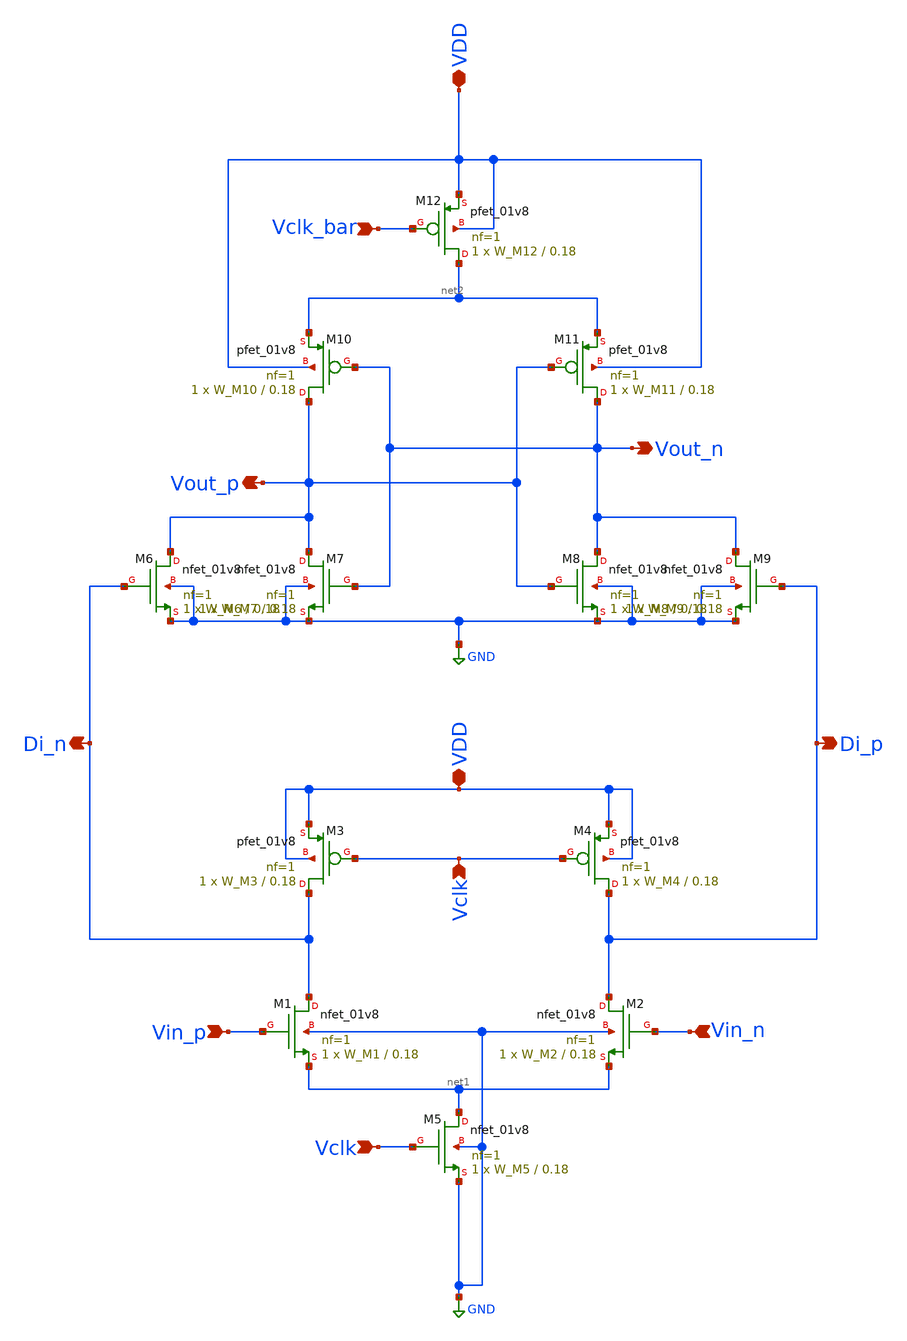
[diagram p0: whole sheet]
** sch_path: xschem/double_tail_comp.sch
**.subckt double_tail_comp VDD Vclk Vclk Vin_p Vin_n Di_n Di_p Vout_n Vout_p Vclk_bar VDD
*.iopin VDD
*.ipin Vclk
*.ipin Vclk
*.ipin Vin_p
*.ipin Vin_n
*.opin Di_n
*.opin Di_p
*.opin Vout_n
*.opin Vout_p
*.ipin Vclk_bar
*.iopin VDD
XM1 Di_n Vin_p net1 GND sky130_fd_pr__nfet_01v8 L=0.18 W=W_M1 nf=1 ad='int((nf+1)/2) * W/nf * 0.29' as='int((nf+2)/2) * W/nf * 0.29'
+ pd='2*int((nf+1)/2) * (W/nf + 0.29)' ps='2*int((nf+2)/2) * (W/nf + 0.29)' nrd='0.29 / W' nrs='0.29 / W'
+ sa=0 sb=0 sd=0 mult=1 m=1
XM2 Di_p Vin_n net1 GND sky130_fd_pr__nfet_01v8 L=0.18 W=W_M2 nf=1 ad='int((nf+1)/2) * W/nf * 0.29' as='int((nf+2)/2) * W/nf * 0.29'
+ pd='2*int((nf+1)/2) * (W/nf + 0.29)' ps='2*int((nf+2)/2) * (W/nf + 0.29)' nrd='0.29 / W' nrs='0.29 / W'
+ sa=0 sb=0 sd=0 mult=1 m=1
XM3 Di_n Vclk VDD VDD sky130_fd_pr__pfet_01v8 L=0.18 W=W_M3 nf=1 ad='int((nf+1)/2) * W/nf * 0.29' as='int((nf+2)/2) * W/nf * 0.29'
+ pd='2*int((nf+1)/2) * (W/nf + 0.29)' ps='2*int((nf+2)/2) * (W/nf + 0.29)' nrd='0.29 / W' nrs='0.29 / W'
+ sa=0 sb=0 sd=0 mult=1 m=1
XM4 Di_p Vclk VDD VDD sky130_fd_pr__pfet_01v8 L=0.18 W=W_M4 nf=1 ad='int((nf+1)/2) * W/nf * 0.29' as='int((nf+2)/2) * W/nf * 0.29'
+ pd='2*int((nf+1)/2) * (W/nf + 0.29)' ps='2*int((nf+2)/2) * (W/nf + 0.29)' nrd='0.29 / W' nrs='0.29 / W'
+ sa=0 sb=0 sd=0 mult=1 m=1
XM5 net1 Vclk GND GND sky130_fd_pr__nfet_01v8 L=0.18 W=W_M5 nf=1 ad='int((nf+1)/2) * W/nf * 0.29' as='int((nf+2)/2) * W/nf * 0.29'
+ pd='2*int((nf+1)/2) * (W/nf + 0.29)' ps='2*int((nf+2)/2) * (W/nf + 0.29)' nrd='0.29 / W' nrs='0.29 / W'
+ sa=0 sb=0 sd=0 mult=1 m=1
XM6 Vout_p Di_n GND GND sky130_fd_pr__nfet_01v8 L=0.18 W=W_M6 nf=1 ad='int((nf+1)/2) * W/nf * 0.29' as='int((nf+2)/2) * W/nf * 0.29'
+ pd='2*int((nf+1)/2) * (W/nf + 0.29)' ps='2*int((nf+2)/2) * (W/nf + 0.29)' nrd='0.29 / W' nrs='0.29 / W'
+ sa=0 sb=0 sd=0 mult=1 m=1
XM7 Vout_p Vout_n GND GND sky130_fd_pr__nfet_01v8 L=0.18 W=W_M7 nf=1 ad='int((nf+1)/2) * W/nf * 0.29'
+ as='int((nf+2)/2) * W/nf * 0.29' pd='2*int((nf+1)/2) * (W/nf + 0.29)' ps='2*int((nf+2)/2) * (W/nf + 0.29)'
+ nrd='0.29 / W' nrs='0.29 / W' sa=0 sb=0 sd=0 mult=1 m=1
XM8 Vout_n Vout_p GND GND sky130_fd_pr__nfet_01v8 L=0.18 W=W_M8 nf=1 ad='int((nf+1)/2) * W/nf * 0.29'
+ as='int((nf+2)/2) * W/nf * 0.29' pd='2*int((nf+1)/2) * (W/nf + 0.29)' ps='2*int((nf+2)/2) * (W/nf + 0.29)'
+ nrd='0.29 / W' nrs='0.29 / W' sa=0 sb=0 sd=0 mult=1 m=1
XM9 Vout_n Di_p GND GND sky130_fd_pr__nfet_01v8 L=0.18 W=W_M9 nf=1 ad='int((nf+1)/2) * W/nf * 0.29' as='int((nf+2)/2) * W/nf * 0.29'
+ pd='2*int((nf+1)/2) * (W/nf + 0.29)' ps='2*int((nf+2)/2) * (W/nf + 0.29)' nrd='0.29 / W' nrs='0.29 / W'
+ sa=0 sb=0 sd=0 mult=1 m=1
XM10 Vout_p Vout_n net2 VDD sky130_fd_pr__pfet_01v8 L=0.18 W=W_M10 nf=1 ad='int((nf+1)/2) * W/nf * 0.29'
+ as='int((nf+2)/2) * W/nf * 0.29' pd='2*int((nf+1)/2) * (W/nf + 0.29)' ps='2*int((nf+2)/2) * (W/nf + 0.29)'
+ nrd='0.29 / W' nrs='0.29 / W' sa=0 sb=0 sd=0 mult=1 m=1
XM11 Vout_n Vout_p net2 VDD sky130_fd_pr__pfet_01v8 L=0.18 W=W_M11 nf=1 ad='int((nf+1)/2) * W/nf * 0.29'
+ as='int((nf+2)/2) * W/nf * 0.29' pd='2*int((nf+1)/2) * (W/nf + 0.29)' ps='2*int((nf+2)/2) * (W/nf + 0.29)'
+ nrd='0.29 / W' nrs='0.29 / W' sa=0 sb=0 sd=0 mult=1 m=1
XM12 net2 Vclk_bar VDD VDD sky130_fd_pr__pfet_01v8 L=0.18 W=W_M12 nf=1 ad='int((nf+1)/2) * W/nf * 0.29'
+ as='int((nf+2)/2) * W/nf * 0.29' pd='2*int((nf+1)/2) * (W/nf + 0.29)' ps='2*int((nf+2)/2) * (W/nf + 0.29)'
+ nrd='0.29 / W' nrs='0.29 / W' sa=0 sb=0 sd=0 mult=1 m=1
**.ends
.GLOBAL GND
.end
